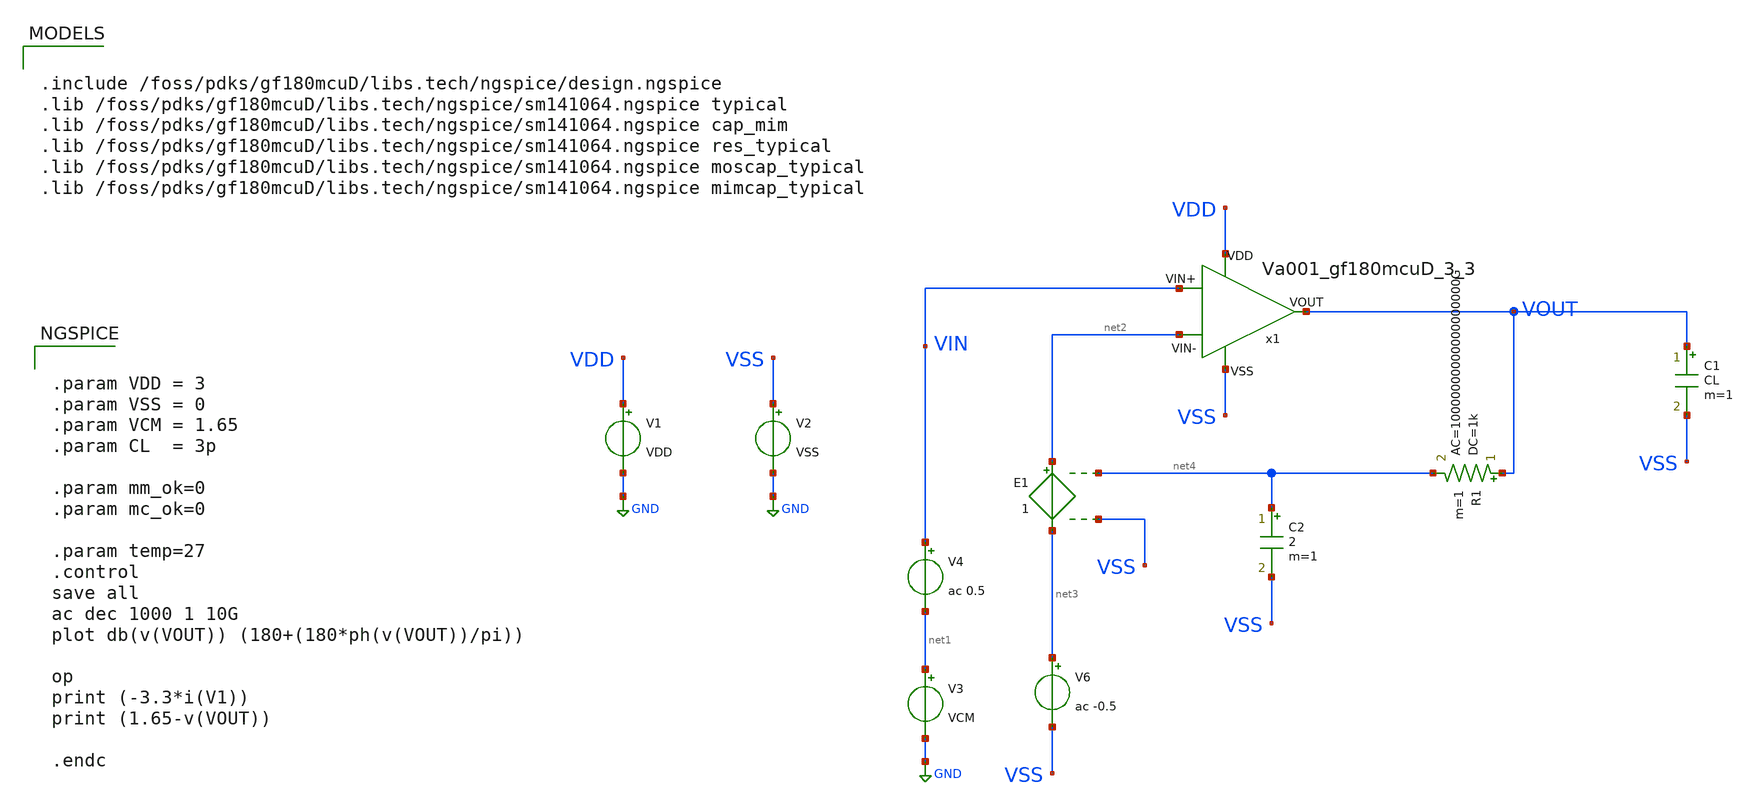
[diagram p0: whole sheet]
** sch_path: Learning/single_ended_amplifiers/VA001_series/Design_and_Analysis_of_Two-Stage_CMOS_Operational_Amplifier_for_Fluorescence_Signal_Processing_gf180mcu_3_3V/amplifier_design/single_tb.sch
**.subckt single_tb
V1 VDD GND VDD
V2 VSS GND VSS
V3 net1 GND VCM
V4 VIN net1 ac 0.5
V6 net3 VSS ac -0.5
C1 VOUT VSS CL m=1
R1 VOUT net4 1k ac=10000000000000000000G m=1
C2 net4 VSS 2 m=1
E1 net2 net3 net4 VSS 1
x1 VDD VSS net2 VIN VOUT Va001_gf180mcuD_3_3
**** begin user architecture code

.include /foss/pdks/gf180mcuD/libs.tech/ngspice/design.ngspice
.lib /foss/pdks/gf180mcuD/libs.tech/ngspice/sm141064.ngspice typical
.lib /foss/pdks/gf180mcuD/libs.tech/ngspice/sm141064.ngspice cap_mim
.lib /foss/pdks/gf180mcuD/libs.tech/ngspice/sm141064.ngspice res_typical
.lib /foss/pdks/gf180mcuD/libs.tech/ngspice/sm141064.ngspice moscap_typical
.lib /foss/pdks/gf180mcuD/libs.tech/ngspice/sm141064.ngspice mimcap_typical

**** end user architecture code
**.ends
.GLOBAL GND
**** begin user architecture code


.param VDD = 3
.param VSS = 0
.param VCM = 1.65
.param CL  = 3p

.param mm_ok=0
.param mc_ok=0

.param temp=27
.control
save all
ac dec 1000 1 10G
plot db(v(VOUT)) (180+(180*ph(v(VOUT))/pi))

op
print (-3.3*i(V1))
print (1.65-v(VOUT))

.endc


**** end user architecture code
.end
